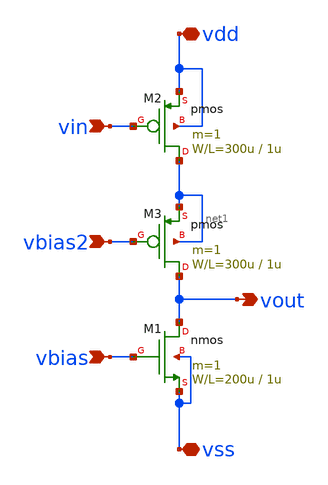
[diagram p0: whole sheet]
** sch_path: pfet_cascode_common_source_load_current.sch
**.subckt pfet_cascode_common_source_load_current vss vdd vin vout vbias vbias2
*.iopin vss
*.iopin vdd
*.ipin vin
*.opin vout
*.ipin vbias
*.ipin vbias2
M1 vout vbias vss vss nmos L=1u W=200u m=1
M2 net1 vin vdd vdd pmos L=1u W=300u m=1
M3 vout vbias2 net1 net1 pmos L=1u W=300u m=1
**** begin user architecture code
 .include $::LIB/mos.lib
.include $::LIB/passive.lib
.include $::LIB/diode.lib
**** end user architecture code
**.ends
.end
